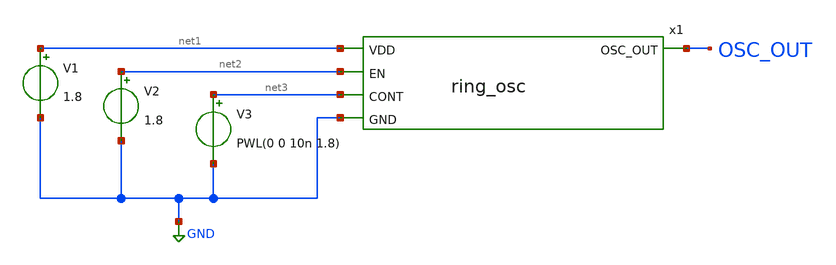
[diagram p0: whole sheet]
** sch_path: xschem/ring_osc/ring_osc_tb.sch
**.subckt ring_osc_tb
x1 net1 net2 OSC_OUT net3 GND ring_osc
V1 net1 GND 1.8
V2 net2 GND 1.8
V3 net3 GND PWL(0 0 10n 1.8)
**.ends
.GLOBAL GND
.end
